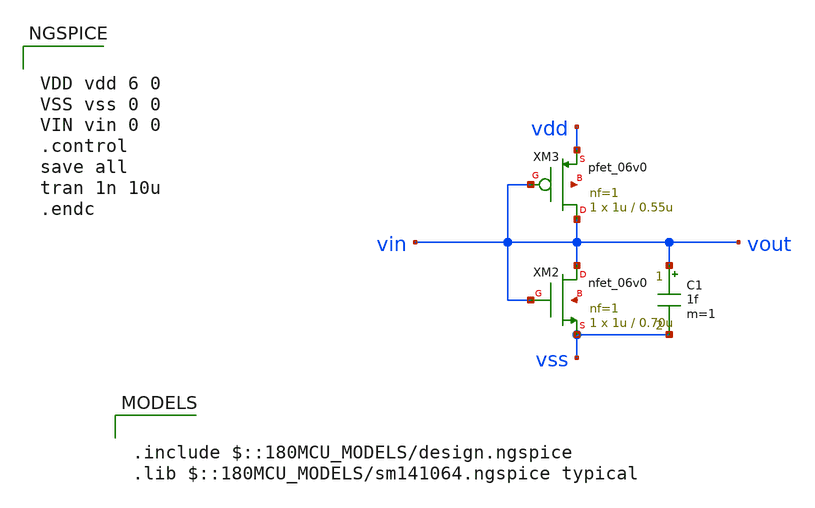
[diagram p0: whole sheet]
** sch_path: xschem/gf_test/inv_tyoketu.sch
**.subckt inv_tyoketu
XM2 vin vin vss net1 nfet_06v0 L=0.70u W=1u nf=1 ad='int((nf+1)/2) * W/nf * 0.18u' as='int((nf+2)/2) * W/nf * 0.18u'
+ pd='2*int((nf+1)/2) * (W/nf + 0.18u)' ps='2*int((nf+2)/2) * (W/nf + 0.18u)' nrd='0.18u / W' nrs='0.18u / W'
+ sa=0 sb=0 sd=0 m=1
XM3 vin vin vdd net2 pfet_06v0 L=0.55u W=1u nf=1 ad='int((nf+1)/2) * W/nf * 0.18u' as='int((nf+2)/2) * W/nf * 0.18u'
+ pd='2*int((nf+1)/2) * (W/nf + 0.18u)' ps='2*int((nf+2)/2) * (W/nf + 0.18u)' nrd='0.18u / W' nrs='0.18u / W'
+ sa=0 sb=0 sd=0 m=1
C1 vin vss 1f m=1
**** begin user architecture code

.include $::180MCU_MODELS/design.ngspice
.lib $::180MCU_MODELS/sm141064.ngspice typical



VDD vdd 6 0
VSS vss 0 0
VIN vin 0 0
.control
save all
tran 1n 10u
.endc


**** end user architecture code
**.ends
.end
